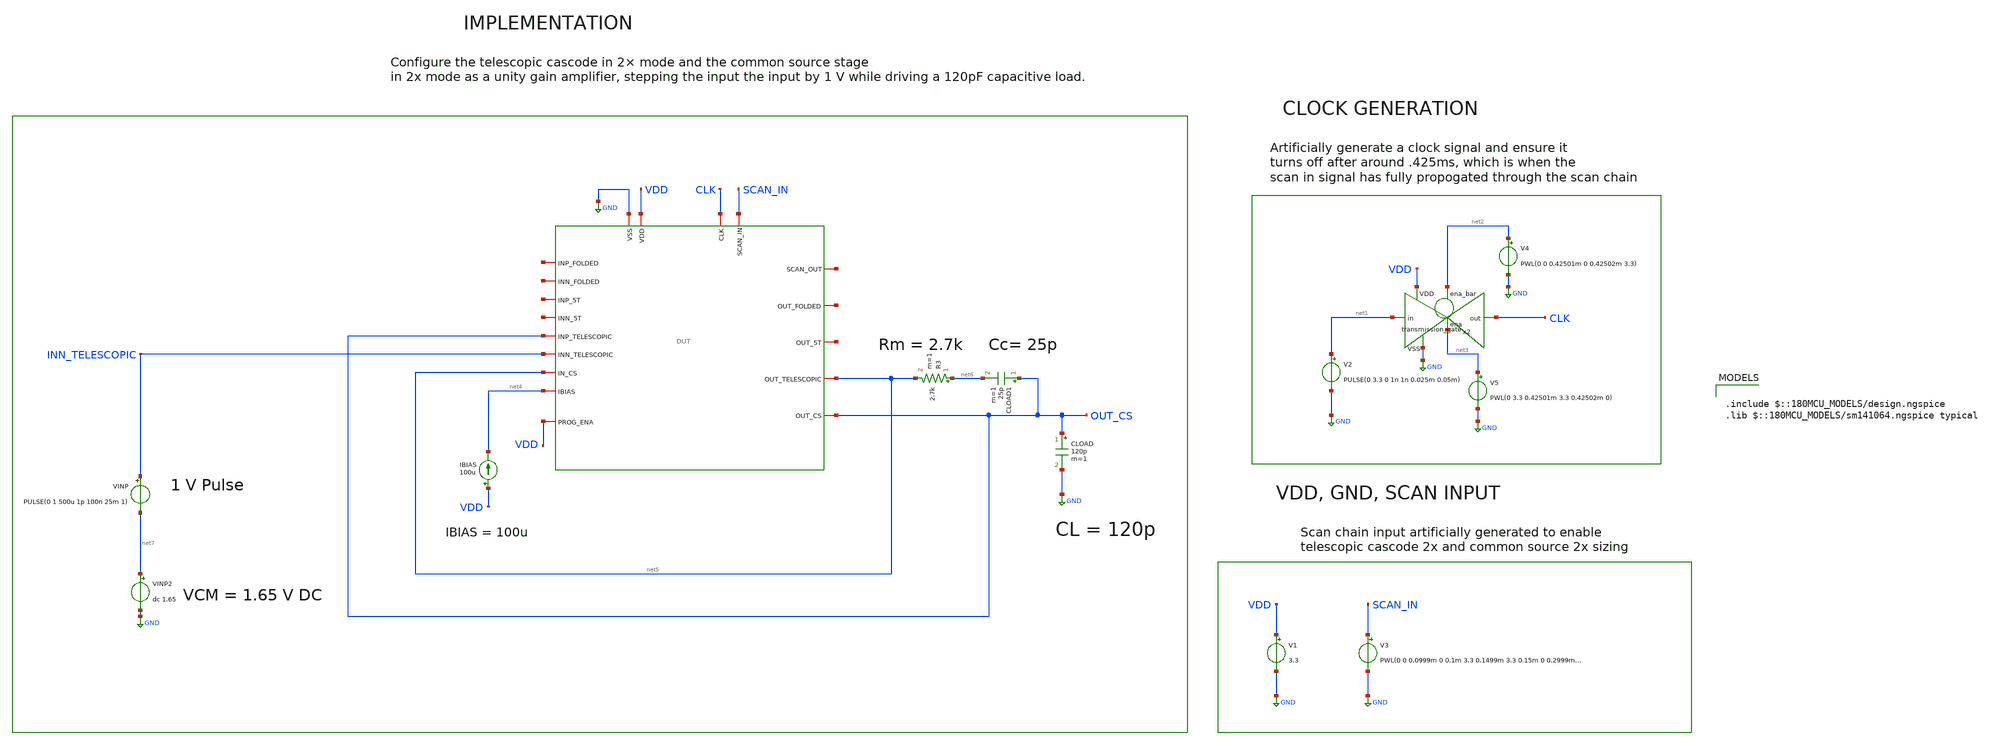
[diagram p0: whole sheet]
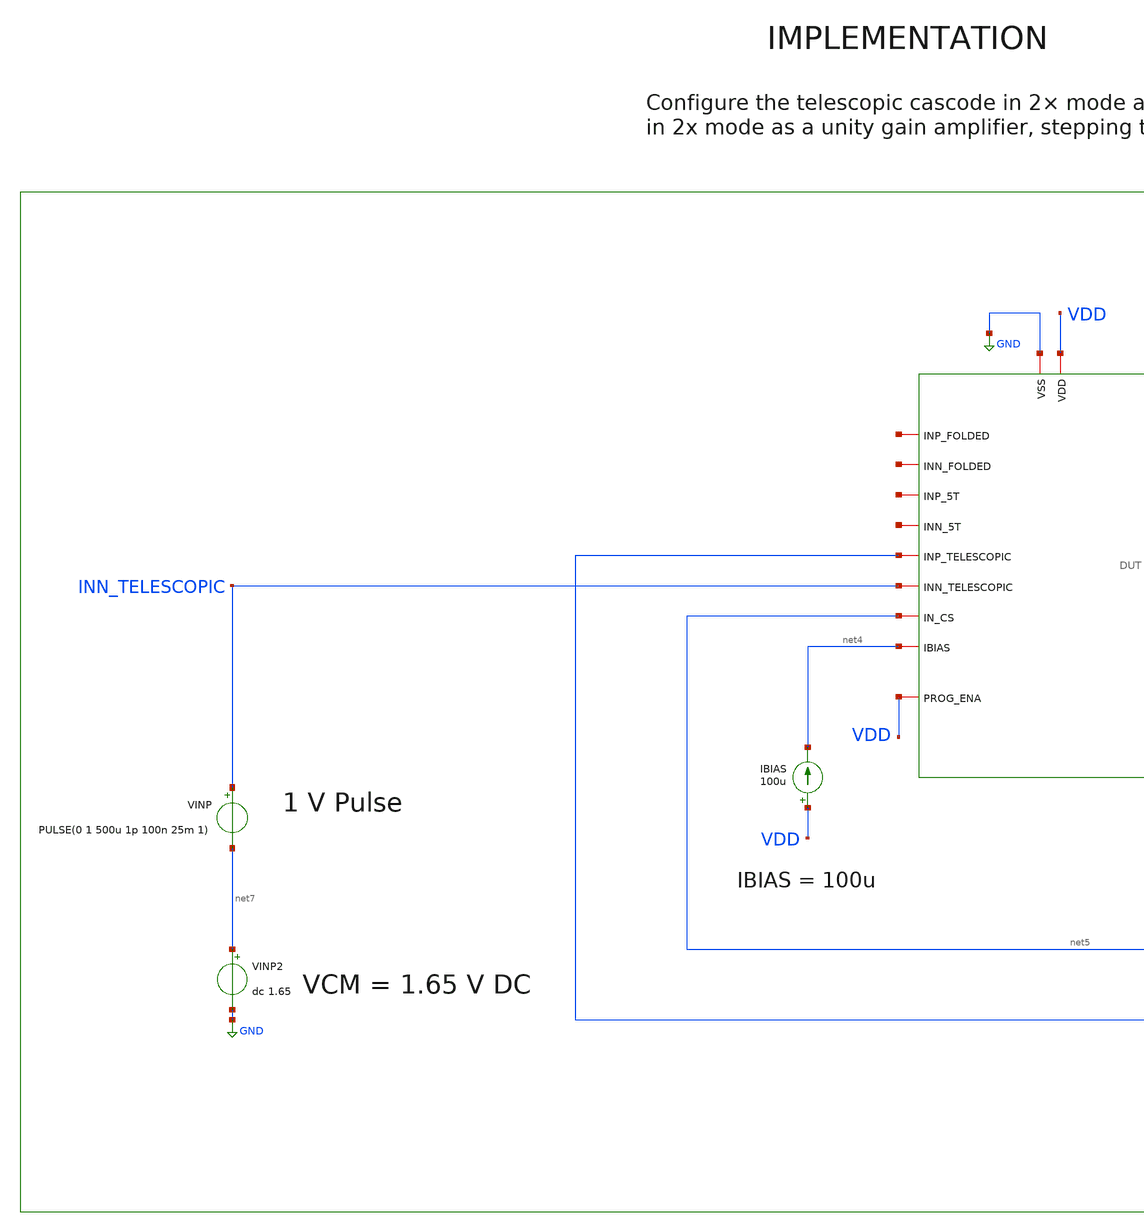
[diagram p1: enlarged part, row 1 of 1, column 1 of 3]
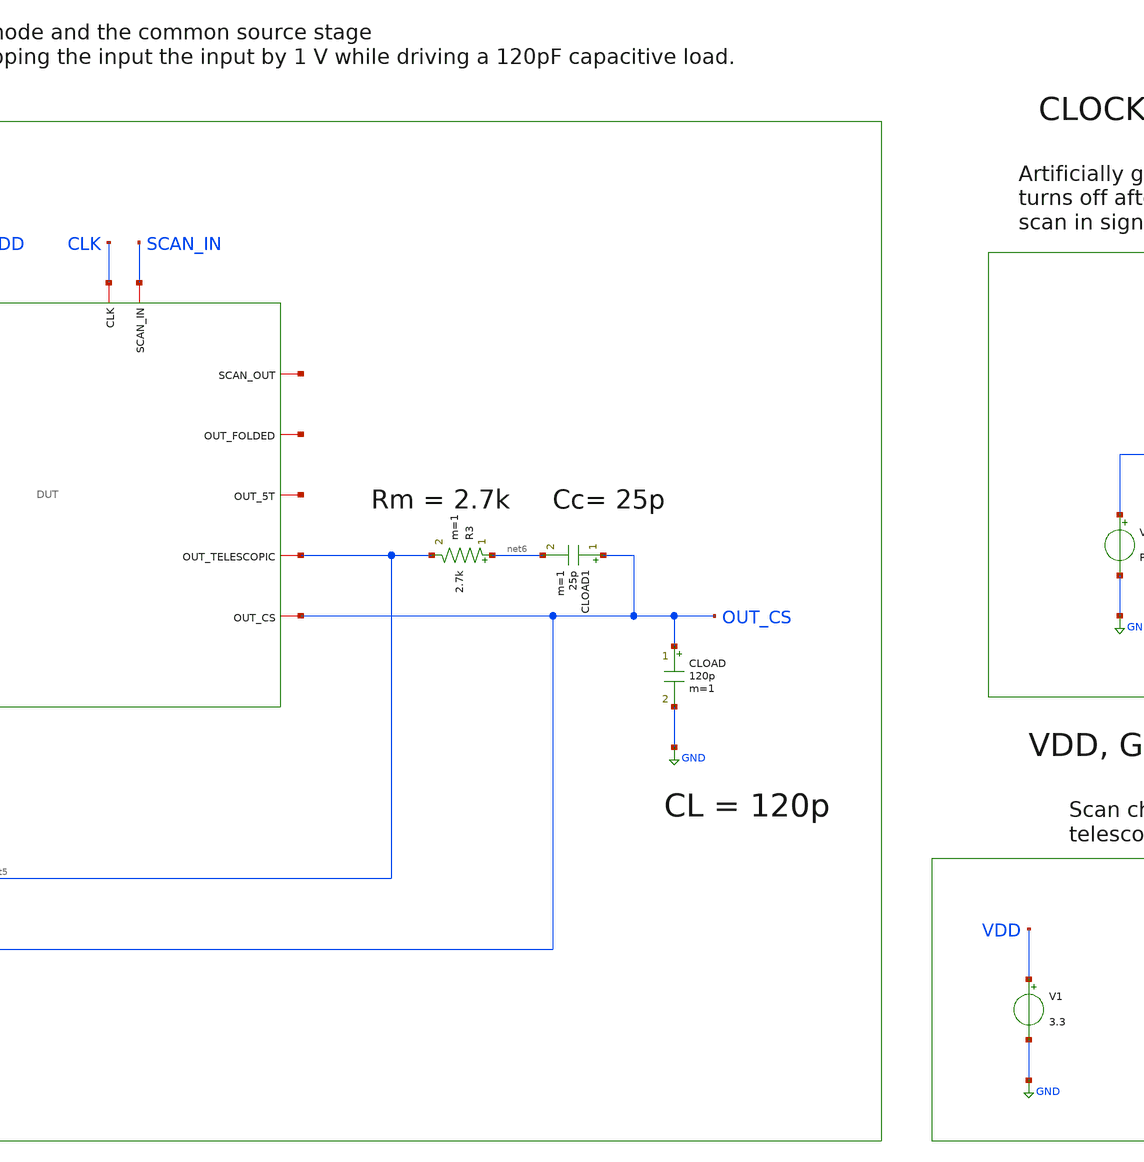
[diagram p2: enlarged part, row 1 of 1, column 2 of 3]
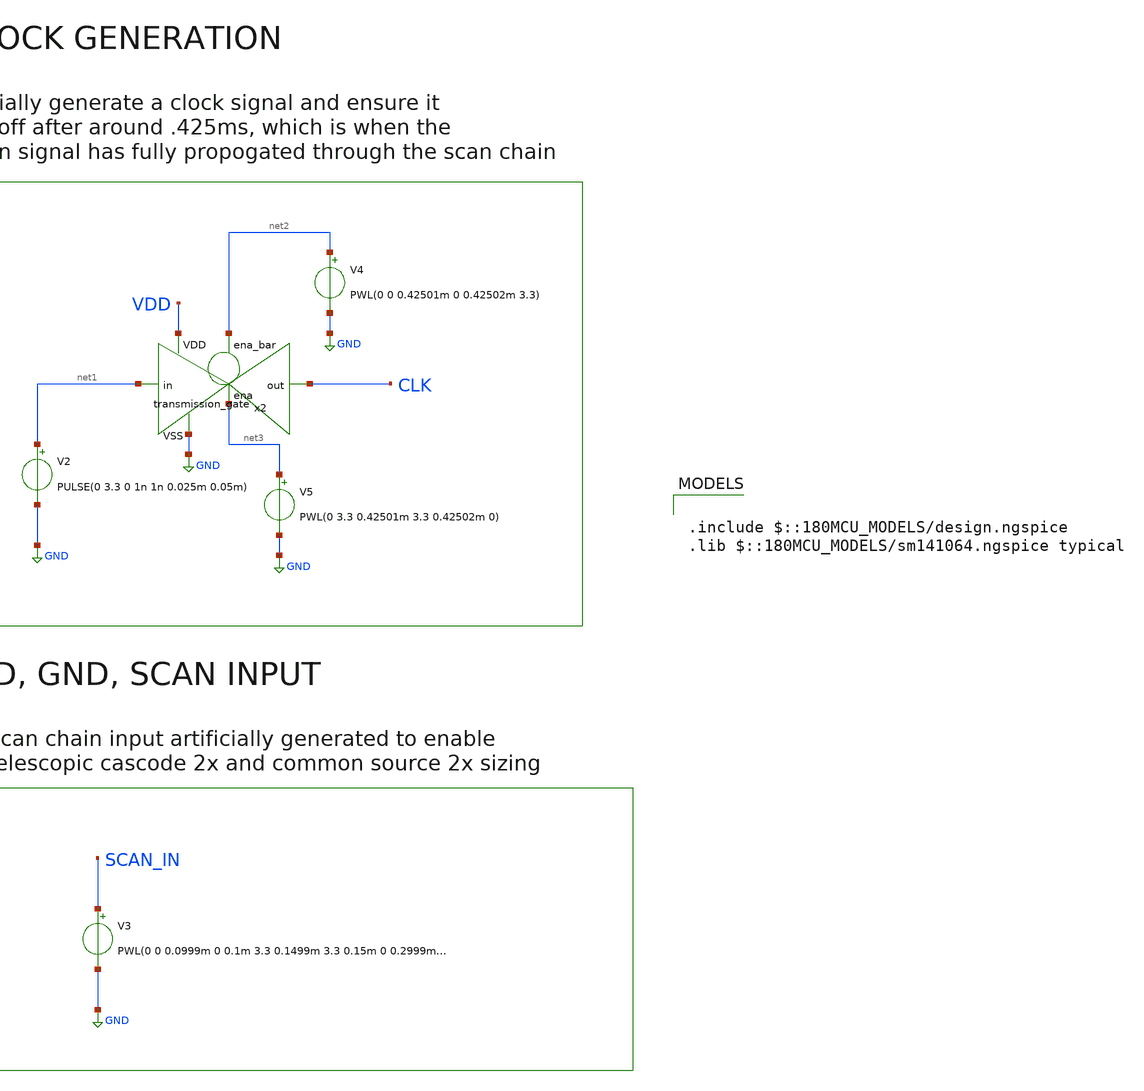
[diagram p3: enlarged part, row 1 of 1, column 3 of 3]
** sch_path: designs/libs/core_tb/mpg/ota_telescopic/2stage/Telescopic_CS_Unity Step/1V_Step_2x_2x_tb.sch
**.subckt 1V_Step_2x_2x_tb
V3 SCAN_IN GND PWL(0 0 0.0999m 0 0.1m 3.3 0.1499m 3.3 0.15m 0 0.2999m 0 0.3m 3.3 0.349999m 3.3 0.35m
+ 0)
V1 VDD GND 3.3
V2 net1 GND PULSE(0 3.3 0 1n 1n 0.025m 0.05m)
x2 net2 VDD CLK net1 GND net3 transmission_gate
V4 net2 GND PWL(0 0 0.42501m 0 0.42502m 3.3)
V5 net3 GND PWL(0 3.3 0.42501m 3.3 0.42502m 0)
IBIAS VDD net4 100u
CLOAD OUT_CS GND 120p m=1
R3 net6 net5 2.7k m=1
CLOAD1 OUT_CS net6 25p m=1
x1 CLK net8 SCAN_IN GND VDD net9 net10 net11 net4 net12 net13 net14 OUT_CS net5 OUT_CS net5
+ INN_TELESCOPIC VDD DUT
VINP INN_TELESCOPIC net7 PULSE(0 1 500u 1p 100n 25m 1)
VINP2 net7 GND dc 1.65
**** begin user architecture code

.include $::180MCU_MODELS/design.ngspice
.lib $::180MCU_MODELS/sm141064.ngspice typical



.control
set color0 = white
set color1 = black
tran 1u 2m

* Output value before the input step
meas tran v_before find v(OUT_CS) at=475u

* Output value after settling
meas tran v_after find v(OUT_CS) at=1.9m

* Calculate the 20% and 80% levels
let v_20 = v_before + 0.2*(v_after - v_before)
let v_80 = v_before + 0.8*(v_after - v_before)

* Measure crossing times after the 500 us input step
meas tran t_20 when v(OUT_CS)=v_20 rise=1 from=500u
meas tran t_80 when v(OUT_CS)=v_80 rise=1 from=500u

* Calculate slew rate
let slew_rate = (v_80 - v_20)/(t_80 - t_20)

print v_before
print v_after
print slew_rate
* Find the maximum output voltage after the input step
meas tran v_peak MAX v(OUT_CS) from=500u to=1.9m

* Overshoot voltage (peak above final value)
let overshoot = v_peak - v_after

* Percent overshoot for a 1 V step
let percent_overshoot = 100*overshoot/1

* Convert percent overshoot to decimal
let PO = percent_overshoot/100

* Damping ratio from percent overshoot
let zeta = -log(PO)/sqrt(pi*pi + log(PO)*log(PO))

* Phase margin (degrees)
let PM = atan((2*zeta)/sqrt(sqrt(1+4*zeta*zeta*zeta*zeta)-2*zeta*zeta))*180/pi

print v_peak
print overshoot
print percent_overshoot
print PM
plot v(INN_TELESCOPIC) v(OUT_CS)

.endc


**** end user architecture code
**.ends
.GLOBAL GND
.end
